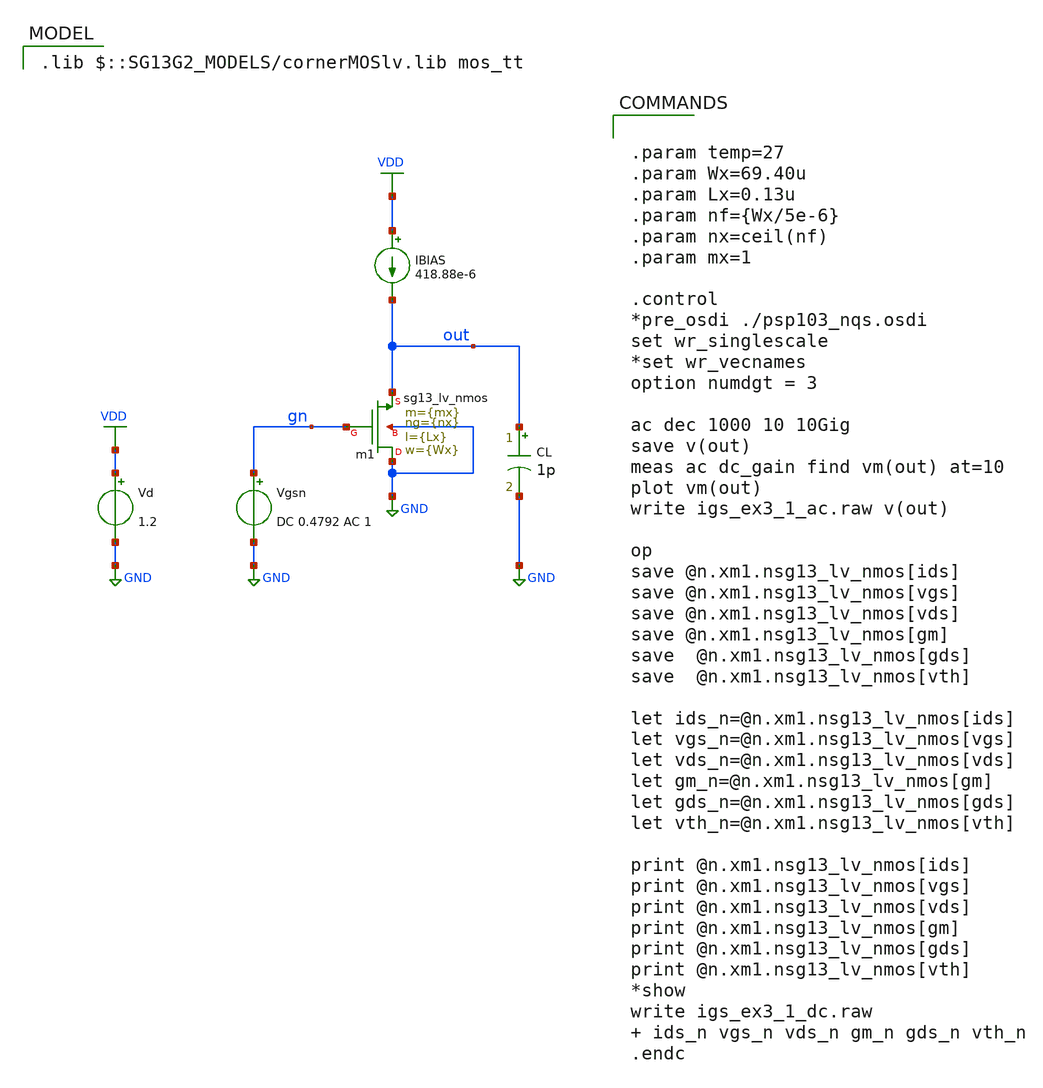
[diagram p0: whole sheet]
** sch_path: 03_design_examples/examples/src/igs_ex3_1.sch
**.subckt igs_ex3_1
Xm1 GND gn out GND sg13_lv_nmos w={Wx} l={Lx} ng={nx} m={mx} mm_ok=1
Vgsn gn GND DC 0.4792 AC 1
Vd VDD GND 1.2
CL out GND 1p m=1
IBIAS VDD out 418.88e-6
**** begin user architecture code
 .lib $::SG13G2_MODELS/cornerMOSlv.lib mos_tt



.param temp=27
.param Wx=69.40u
.param Lx=0.13u
.param nf={Wx/5e-6}
.param nx=ceil(nf)
.param mx=1

.control
*pre_osdi ./psp103_nqs.osdi
set wr_singlescale
*set wr_vecnames
option numdgt = 3

ac dec 1000 10 10Gig
save v(out)
meas ac dc_gain find vm(out) at=10
plot vm(out)
write igs_ex3_1_ac.raw v(out)

op
save @n.xm1.nsg13_lv_nmos[ids]
save @n.xm1.nsg13_lv_nmos[vgs]
save @n.xm1.nsg13_lv_nmos[vds]
save @n.xm1.nsg13_lv_nmos[gm]
save  @n.xm1.nsg13_lv_nmos[gds]
save  @n.xm1.nsg13_lv_nmos[vth]

let ids_n=@n.xm1.nsg13_lv_nmos[ids]
let vgs_n=@n.xm1.nsg13_lv_nmos[vgs]
let vds_n=@n.xm1.nsg13_lv_nmos[vds]
let gm_n=@n.xm1.nsg13_lv_nmos[gm]
let gds_n=@n.xm1.nsg13_lv_nmos[gds]
let vth_n=@n.xm1.nsg13_lv_nmos[vth]

print @n.xm1.nsg13_lv_nmos[ids]
print @n.xm1.nsg13_lv_nmos[vgs]
print @n.xm1.nsg13_lv_nmos[vds]
print @n.xm1.nsg13_lv_nmos[gm]
print @n.xm1.nsg13_lv_nmos[gds]
print @n.xm1.nsg13_lv_nmos[vth]
*show
write igs_ex3_1_dc.raw   ids_n vgs_n vds_n gm_n gds_n vth_n
.endc


**** end user architecture code
**.ends
.GLOBAL GND
.GLOBAL VDD
.end
